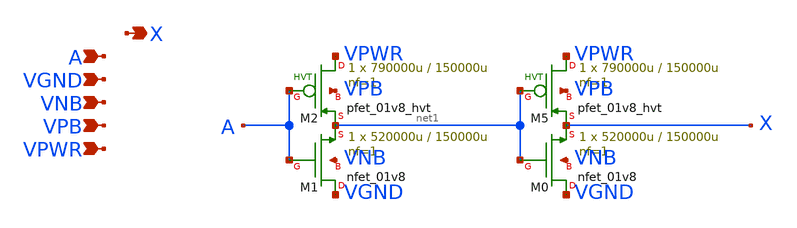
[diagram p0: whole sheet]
** sch_path: schematics/buf/sky130_fd_sc_hd__buf_1.sch
**.subckt sky130_fd_sc_hd__buf_1 A VGND VNB VPB VPWR X
*.ipin A
*.ipin VGND
*.ipin VNB
*.ipin VPB
*.ipin VPWR
*.opin X
XM0 VGND net1 X VNB sky130_fd_pr__nfet_01v8 L=150000u W=520000u nf=1 ad='int((1 + 1)/2) * 520000u / 1 * 0.29'
+ as='int((1 + 2)/2) * 520000u / 1 * 0.29' pd='2*int((1 + 1)/2) * (520000u / 1 + 0.29)' ps='2*int((1 + 2)/2) * (520000u / 1 + 0.29)'
+ nrd='0.29 / 520000u ' nrs='0.29 / 520000u ' sa=0 sb=0 sd=0 mult=1 m=1
XM5 VPWR net1 X VPB sky130_fd_pr__pfet_01v8_hvt L=150000u W=790000u nf=1 ad='int((1 + 1)/2) * 790000u / 1 * 0.29'
+ as='int((1 + 2)/2) * 790000u / 1 * 0.29' pd='2*int((1 + 1)/2) * (790000u / 1 + 0.29)' ps='2*int((1 + 2)/2) * (790000u / 1 + 0.29)'
+ nrd='0.29 / 790000u ' nrs='0.29 / 790000u ' sa=0 sb=0 sd=0 mult=1 m=1
XM1 VGND A net1 VNB sky130_fd_pr__nfet_01v8 L=150000u W=520000u nf=1 ad='int((1 + 1)/2) * 520000u / 1 * 0.29'
+ as='int((1 + 2)/2) * 520000u / 1 * 0.29' pd='2*int((1 + 1)/2) * (520000u / 1 + 0.29)' ps='2*int((1 + 2)/2) * (520000u / 1 + 0.29)'
+ nrd='0.29 / 520000u ' nrs='0.29 / 520000u ' sa=0 sb=0 sd=0 mult=1 m=1
XM2 VPWR A net1 VPB sky130_fd_pr__pfet_01v8_hvt L=150000u W=790000u nf=1 ad='int((1 + 1)/2) * 790000u / 1 * 0.29'
+ as='int((1 + 2)/2) * 790000u / 1 * 0.29' pd='2*int((1 + 1)/2) * (790000u / 1 + 0.29)' ps='2*int((1 + 2)/2) * (790000u / 1 + 0.29)'
+ nrd='0.29 / 790000u ' nrs='0.29 / 790000u ' sa=0 sb=0 sd=0 mult=1 m=1
**.ends
.end
